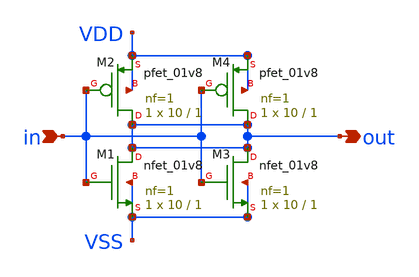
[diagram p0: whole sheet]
** sch_path: tt_um_wulf_8bit_vco/xschem/lib/buf_md.sch
**.subckt buf_md out in
*.opin out
*.ipin in
XM1 out in VSS VSS sky130_fd_pr__nfet_01v8 L=1 W=10 nf=1 ad='int((1 + 1)/2) * 10 / 1 * 0.29' as='int((1 + 2)/2) * 10 / 1 * 0.29'
+ pd='2*int((1 + 1)/2) * (10 / 1 + 0.29)' ps='2*int((1 + 2)/2) * (10 / 1 + 0.29)' nrd='0.29 / 10 ' nrs='0.29 / 10 '
+ sa=0 sb=0 sd=0 mult=1 m=1
XM2 out in VDD VDD sky130_fd_pr__pfet_01v8 L=1 W=10 nf=1 ad='int((nf+1)/2) * W/nf * 0.29' as='int((nf+2)/2) * W/nf * 0.29'
+ pd='2*int((nf+1)/2) * (W/nf + 0.29)' ps='2*int((nf+2)/2) * (W/nf + 0.29)' nrd='0.29 / W' nrs='0.29 / W'
+ sa=0 sb=0 sd=0 mult=1 m=1
XM3 out in VSS VSS sky130_fd_pr__nfet_01v8 L=1 W=10 nf=1 ad='int((1 + 1)/2) * 10 / 1 * 0.29' as='int((1 + 2)/2) * 10 / 1 * 0.29'
+ pd='2*int((1 + 1)/2) * (10 / 1 + 0.29)' ps='2*int((1 + 2)/2) * (10 / 1 + 0.29)' nrd='0.29 / 10 ' nrs='0.29 / 10 '
+ sa=0 sb=0 sd=0 mult=1 m=1
XM4 out in VDD VDD sky130_fd_pr__pfet_01v8 L=1 W=10 nf=1 ad='int((nf+1)/2) * W/nf * 0.29' as='int((nf+2)/2) * W/nf * 0.29'
+ pd='2*int((nf+1)/2) * (W/nf + 0.29)' ps='2*int((nf+2)/2) * (W/nf + 0.29)' nrd='0.29 / W' nrs='0.29 / W'
+ sa=0 sb=0 sd=0 mult=1 m=1
**.ends
.end
